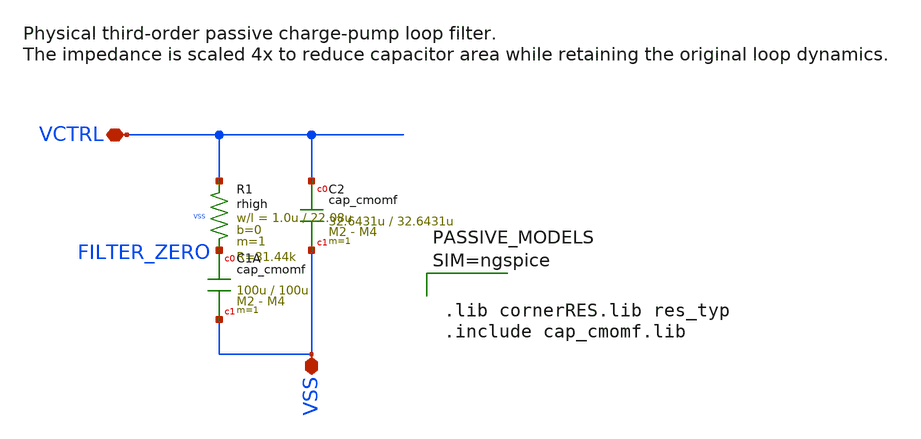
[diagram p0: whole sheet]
** sch_path: macros/pll_analog/schematic/xschem/loop_filter.sch
**.subckt loop_filter VCTRL VSS
*.iopin VCTRL
*.iopin VSS
XR1 VCTRL FILTER_ZERO VSS rhigh w=1.0u l=22.08u m=1 b=0 mm_ok=1
XC1A FILTER_ZERO VSS cap_cmomf w=100u l=100u mmin=2 mmax=4 subblock=0 rfmodel=0 subscale=1 m=1
+ mm_ok=1
XC2 VCTRL VSS cap_cmomf w=32.6431u l=32.6431u mmin=2 mmax=4 subblock=0 rfmodel=0 subscale=1 m=1
+ mm_ok=1
**** begin user architecture code



.lib cornerRES.lib res_typ
.include cap_cmomf.lib



**** end user architecture code
**.ends
.end
